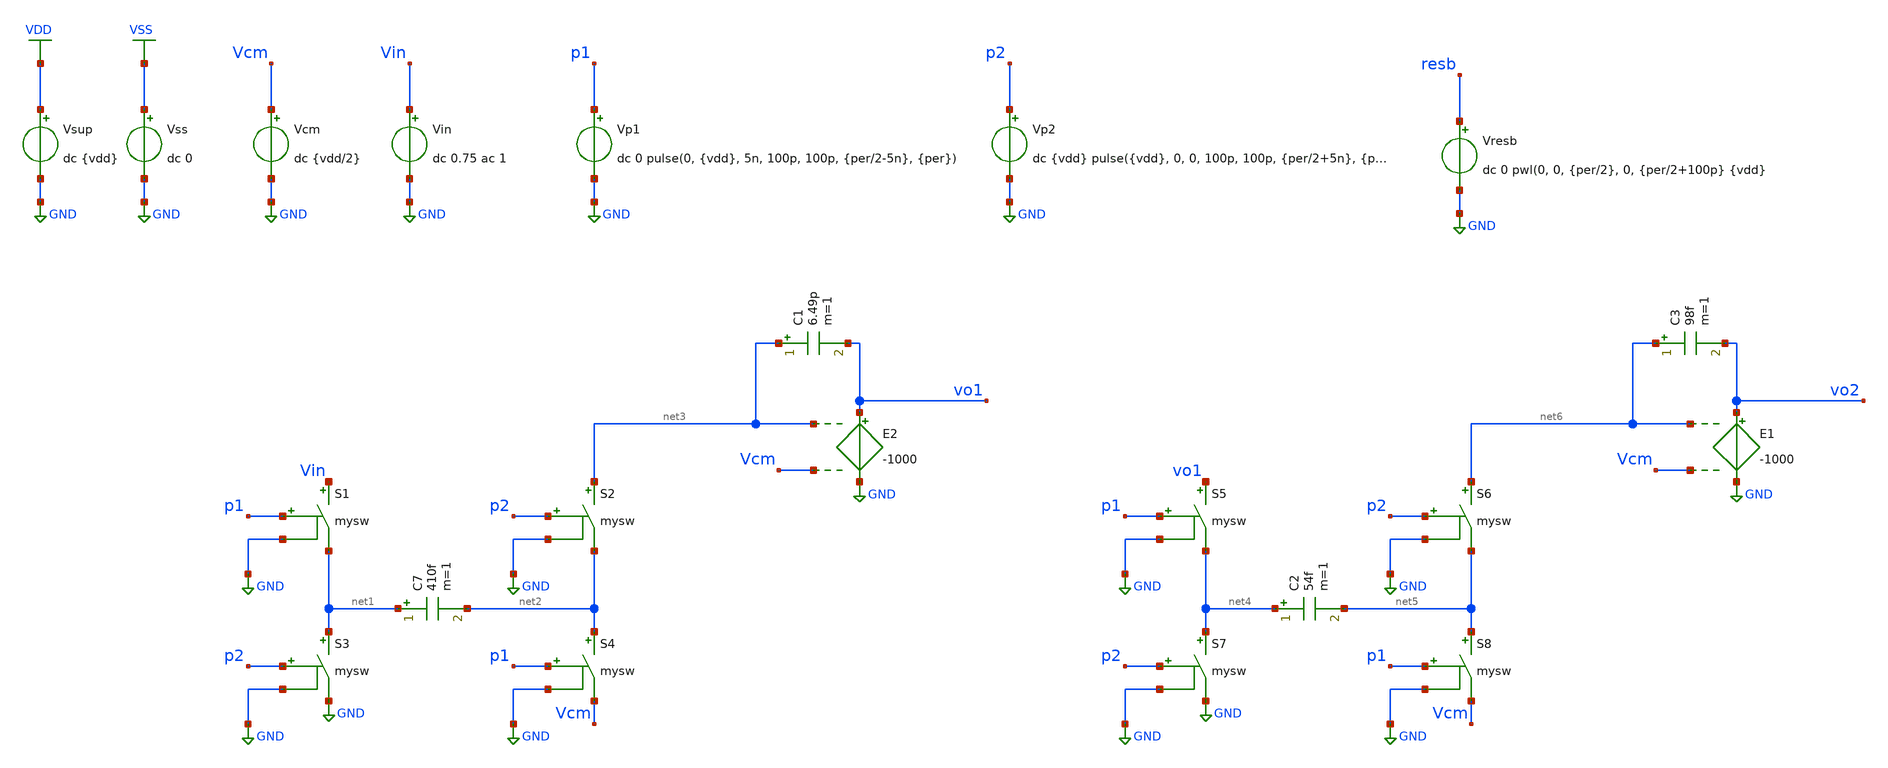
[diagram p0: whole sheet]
** sch_path: DSM/IC_Designs_Hrishi/IdealCircuits/IdealSwitchCapacitor_VCVS.sch
**.subckt IdealSwitchCapacitor_VCVS
Vcm Vcm GND dc {vdd/2}
Vin Vin GND dc 0.75 ac 1
Vp1 p1 GND dc 0 pulse(0, {vdd}, 5n, 100p, 100p, {per/2-5n}, {per})
Vp2 p2 GND dc {vdd} pulse({vdd}, 0, 0, 100p, 100p, {per/2+5n}, {per})
S1 Vin net1 p1 GND mysw
S2 net3 net2 p2 GND mysw
S3 net1 GND p2 GND mysw
S4 net2 Vcm p1 GND mysw
C7 net1 net2 410f m=1
C1 net3 vo1 6.49p m=1
Vresb resb GND dc 0 pwl(0, 0, {per/2}, 0, {per/2+100p} {vdd}
Vsup VDD GND dc {vdd}
Vss VSS GND dc 0
S5 vo1 net4 p1 GND mysw
S6 net6 net5 p2 GND mysw
S7 net4 GND p2 GND mysw
S8 net5 Vcm p1 GND mysw
C2 net4 net5 54f m=1
C3 net6 vo2 98f m=1
E2 vo1 GND net3 Vcm -1000
E1 vo2 GND net6 Vcm -1000
**** begin user architecture code

.lib $::SG13G2_MODELS/cornerMOSlv.lib mos_tt
.lib $::SG13G2_MODELS/cornerRES.lib res_typ
.inc /foss/pdks/sg13g2/libs.ref/sg13g2_stdcell/spice/sg13g2_stdcell.spice



.param temp=27 vdd = 1.8 per=1u
.model mysw SW vt={vdd/2} ron=0.1
.option method=gear reltol=1e-4

.control
save all
run
tran 10n 30u
plot vo1 vo2
set wr_singlescale
set wr_vecnames
wrdata IDEAL_SwitchCap.txt vo1 p1 p2
.endc


**** end user architecture code
**.ends
.GLOBAL GND
.GLOBAL VDD
.GLOBAL VSS
.end
